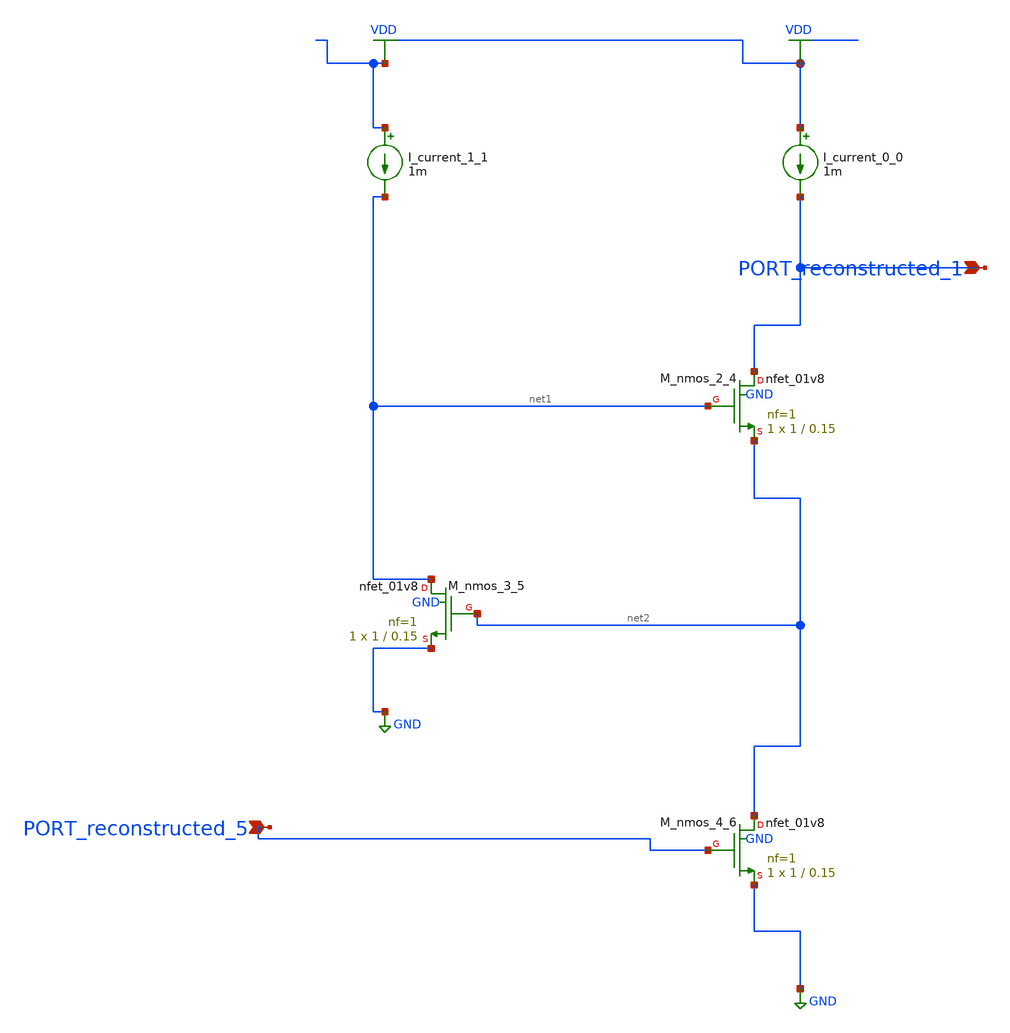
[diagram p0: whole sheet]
** sch_path: schematics/AMSNet/713.sch
**.subckt 713 PORT_reconstructed_1 PORT_reconstructed_5
*.ipin PORT_reconstructed_1
*.ipin PORT_reconstructed_5
I_current_0_0 VDD PORT_reconstructed_1 1m
I_current_1_1 VDD net1 1m
XM_nmos_2_4 PORT_reconstructed_1 net1 net2 GND sky130_fd_pr__nfet_01v8 L=0.15 W=1 nf=1 ad='int((1 + 1)/2) * 1 / 1 * 0.29'
+ as='int((1 + 2)/2) * 1 / 1 * 0.29' pd='2*int((1 + 1)/2) * (1 / 1 + 0.29)' ps='2*int((1 + 2)/2) * (1 / 1 + 0.29)'
+ nrd='0.29 / 1 ' nrs='0.29 / 1 ' sa=0 sb=0 sd=0 mult=1 m=1
XM_nmos_3_5 net1 net2 GND GND sky130_fd_pr__nfet_01v8 L=0.15 W=1 nf=1 ad='int((1 + 1)/2) * 1 / 1 * 0.29'
+ as='int((1 + 2)/2) * 1 / 1 * 0.29' pd='2*int((1 + 1)/2) * (1 / 1 + 0.29)' ps='2*int((1 + 2)/2) * (1 / 1 + 0.29)'
+ nrd='0.29 / 1 ' nrs='0.29 / 1 ' sa=0 sb=0 sd=0 mult=1 m=1
XM_nmos_4_6 net2 PORT_reconstructed_5 GND GND sky130_fd_pr__nfet_01v8 L=0.15 W=1 nf=1 ad='int((1 + 1)/2) * 1 / 1 * 0.29'
+ as='int((1 + 2)/2) * 1 / 1 * 0.29' pd='2*int((1 + 1)/2) * (1 / 1 + 0.29)' ps='2*int((1 + 2)/2) * (1 / 1 + 0.29)'
+ nrd='0.29 / 1 ' nrs='0.29 / 1 ' sa=0 sb=0 sd=0 mult=1 m=1
**.ends
.GLOBAL GND
.GLOBAL VDD
.end
